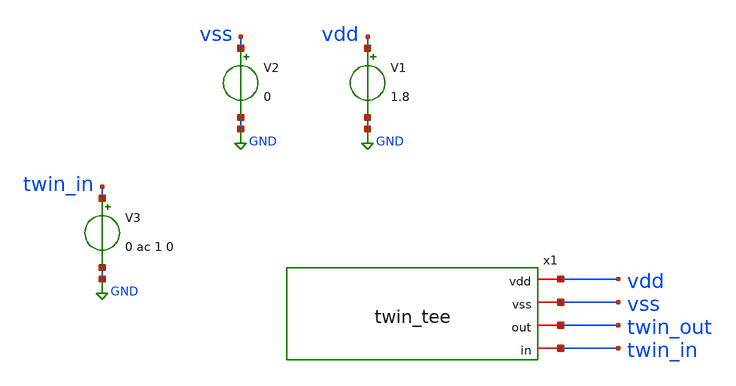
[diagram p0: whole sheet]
** sch_path: xschem/tb_twin_tee.sch
**.subckt tb_twin_tee
V1 vdd GND 1.8
V2 vss GND 0
V3 twin_in GND 0 ac 1 0
x1 vdd vss twin_out twin_in twin_tee
**** begin user architecture code

** opencircuitdesign pdks install
.lib $::SKYWATER_MODELS/sky130.lib.spice tt
.include $::SKYWATER_STDCELLS/sky130_fd_sc_hd.spice





.param mc_mm_switch=0
.control
ac dec 100 1 100e7
*  tran 500p 2u uic
  write testbench.raw
  set appendwrite


.endc


**** end user architecture code
**.ends

* expanding   symbol:  twin_tee.sym # of pins=4
** sym_path: xschem/twin_tee.sym
** sch_path: xschem/twin_tee.sch
.subckt twin_tee vdd vss out in
*.iopin vdd
*.iopin vss
*.iopin in
*.iopin out
XR4 net1 out vss sky130_fd_pr__res_high_po_0p35 L=10 mult=1 m=1
XC1 net1 vss sky130_fd_pr__cap_mim_m3_1 W=15 L=15 MF=1 m=1
XC2 net1 vss sky130_fd_pr__cap_mim_m3_1 W=15 L=15 MF=1 m=1
XR5 in net1 vss sky130_fd_pr__res_high_po_0p35 L=10 mult=1 m=1
XC3 net2 in sky130_fd_pr__cap_mim_m3_1 W=15 L=15 MF=1 m=1
XC4 out net2 sky130_fd_pr__cap_mim_m3_1 W=15 L=15 MF=1 m=1
XR6 net2 vss vss sky130_fd_pr__res_high_po_0p35 L=5 mult=1 m=1
.ends

.GLOBAL GND
.end
